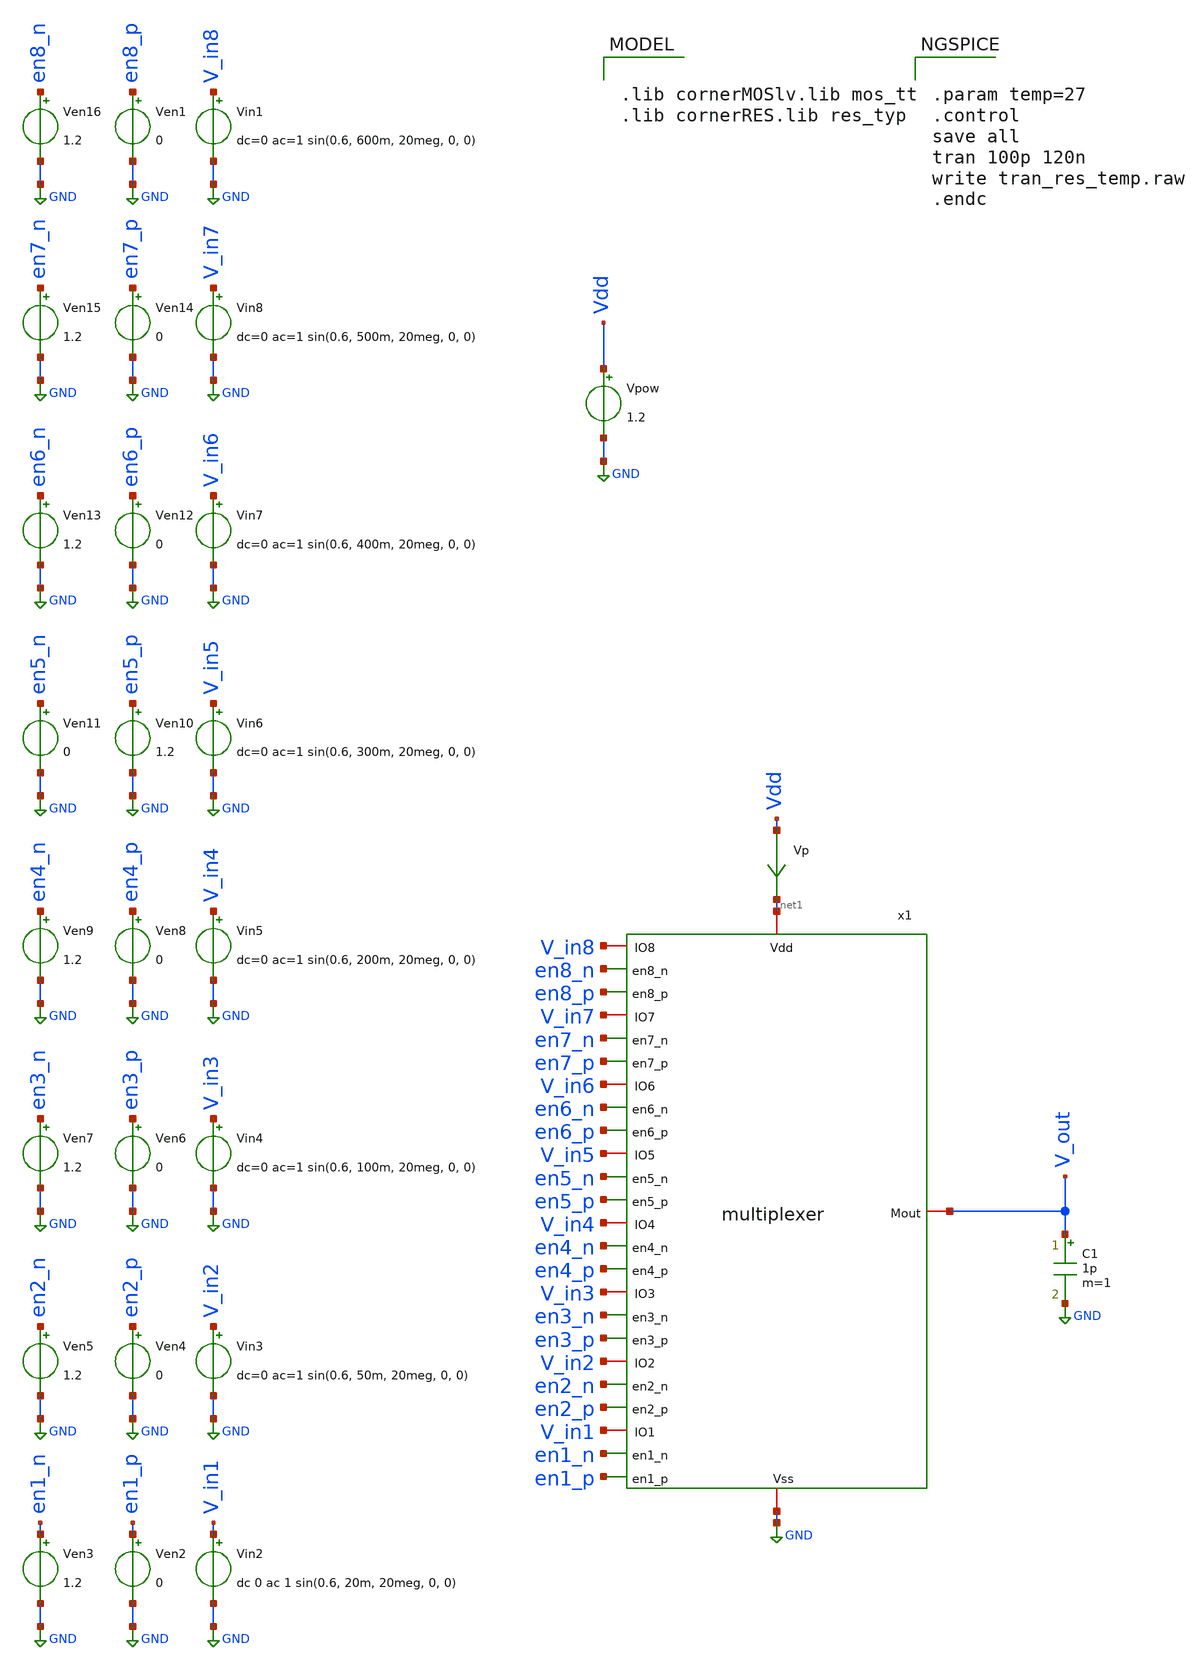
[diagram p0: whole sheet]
** sch_path: CHIPCHILE_CANELOS24_WorkshopTO/design_data/xschem/multiplexer/multiplexer_tb.sch
* Copyright 2023 IHP PDK Authors
**.subckt multiplexer_tb
Vpow Vdd GND 1.2
Vp Vdd net1 0
.save i(vp)
C1 V_out GND 1p m=1
x1 net1 V_in8 en8_n en8_p V_in7 en7_n en7_p V_in6 en6_n en6_p V_in5 en5_n en5_p V_out V_in4 en4_n
+ en4_p V_in3 en3_n en3_p V_in2 en2_n en2_p V_in1 en1_n en1_p GND multiplexer
Ven2 en1_p GND 0
Ven3 en1_n GND 1.2
Vin2 V_in1 GND dc 0 ac 1 sin(0.6, 20m, 20meg, 0, 0)
Ven4 en2_p GND 0
Ven5 en2_n GND 1.2
Vin3 V_in2 GND dc=0 ac=1 sin(0.6, 50m, 20meg, 0, 0)
Ven6 en3_p GND 0
Ven7 en3_n GND 1.2
Vin4 V_in3 GND dc=0 ac=1 sin(0.6, 100m, 20meg, 0, 0)
Ven8 en4_p GND 0
Ven9 en4_n GND 1.2
Vin5 V_in4 GND dc=0 ac=1 sin(0.6, 200m, 20meg, 0, 0)
Ven10 en5_p GND 1.2
Ven11 en5_n GND 0
Vin6 V_in5 GND dc=0 ac=1 sin(0.6, 300m, 20meg, 0, 0)
Ven12 en6_p GND 0
Ven13 en6_n GND 1.2
Vin7 V_in6 GND dc=0 ac=1 sin(0.6, 400m, 20meg, 0, 0)
Ven14 en7_p GND 0
Ven15 en7_n GND 1.2
Vin8 V_in7 GND dc=0 ac=1 sin(0.6, 500m, 20meg, 0, 0)
Ven1 en8_p GND 0
Ven16 en8_n GND 1.2
Vin1 V_in8 GND dc=0 ac=1 sin(0.6, 600m, 20meg, 0, 0)
**** begin user architecture code

.lib cornerMOSlv.lib mos_tt
.lib cornerRES.lib res_typ



.param temp=27
.control
save all
tran 100p 120n
write tran_res_temp.raw
.endc


**** end user architecture code
**.ends

* expanding   symbol:  multiplexer.sym # of pins=27
** sym_path: CHIPCHILE_CANELOS24_WorkshopTO/design_data/xschem/multiplexer/multiplexer.sym
** sch_path: CHIPCHILE_CANELOS24_WorkshopTO/design_data/xschem/multiplexer/multiplexer.sch
.subckt multiplexer Vdd IO8 en8_n en8_p IO7 en7_n en7_p IO6 en6_n en6_p IO5 en5_n en5_p Mout IO4
+ en4_n en4_p IO3 en3_n en3_p IO2 en2_n en2_p IO1 en1_n en1_p Vss
*.iopin IO1
*.iopin Vss
*.ipin en1_n
*.ipin en1_p
*.iopin IO2
*.iopin Mout
*.ipin en2_n
*.ipin en2_p
*.iopin IO3
*.ipin en3_n
*.ipin en3_p
*.iopin IO4
*.ipin en4_n
*.ipin en4_p
*.iopin IO5
*.ipin en5_n
*.ipin en5_p
*.iopin IO6
*.ipin en6_n
*.ipin en6_p
*.iopin IO7
*.ipin en7_n
*.ipin en7_p
*.iopin IO8
*.iopin Vdd
*.ipin en8_n
*.ipin en8_p
x1 Vdd en1_n IO1 Mout en1_p Vss transmission_gate
x2 Vdd en2_n IO2 Mout en2_p Vss transmission_gate
x3 Vdd en3_n IO3 Mout en3_p Vss transmission_gate
x4 Vdd en4_n IO4 Mout en4_p Vss transmission_gate
x5 Vdd en5_n IO5 Mout en5_p Vss transmission_gate
x6 Vdd en6_n IO6 Mout en6_p Vss transmission_gate
x7 Vdd en7_n IO7 Mout en7_p Vss transmission_gate
x8 Vdd en8_n IO8 Mout en8_p Vss transmission_gate
.ends


* expanding   symbol:  transmission_gate.sym # of pins=6
** sym_path: CHIPCHILE_CANELOS24_WorkshopTO/design_data/xschem/multiplexer/transmission_gate.sym
** sch_path: CHIPCHILE_CANELOS24_WorkshopTO/design_data/xschem/multiplexer/transmission_gate.sch
.subckt transmission_gate vdd en_n inout_1 inout_2 en_p vss
*.iopin inout_1
*.iopin inout_2
*.ipin en_p
*.iopin vdd
*.iopin vss
*.ipin en_n
XM1 inout_1 en_p inout_2 net1 sg13_lv_nmos w=200.0u l=0.130u ng=20 m=1 mm_ok=1
XM2 inout_1 en_n inout_2 net2 sg13_lv_pmos w=200.0u l=0.130u ng=20 m=1 mm_ok=1
XR1 vdd net2 ntap1 R=262.8 w=0.78e-6 l=0.78e-6
XR2 vss net1 ptap1 R=262.8 w=0.78e-6 l=0.78e-6
.ends

.GLOBAL GND
.end
